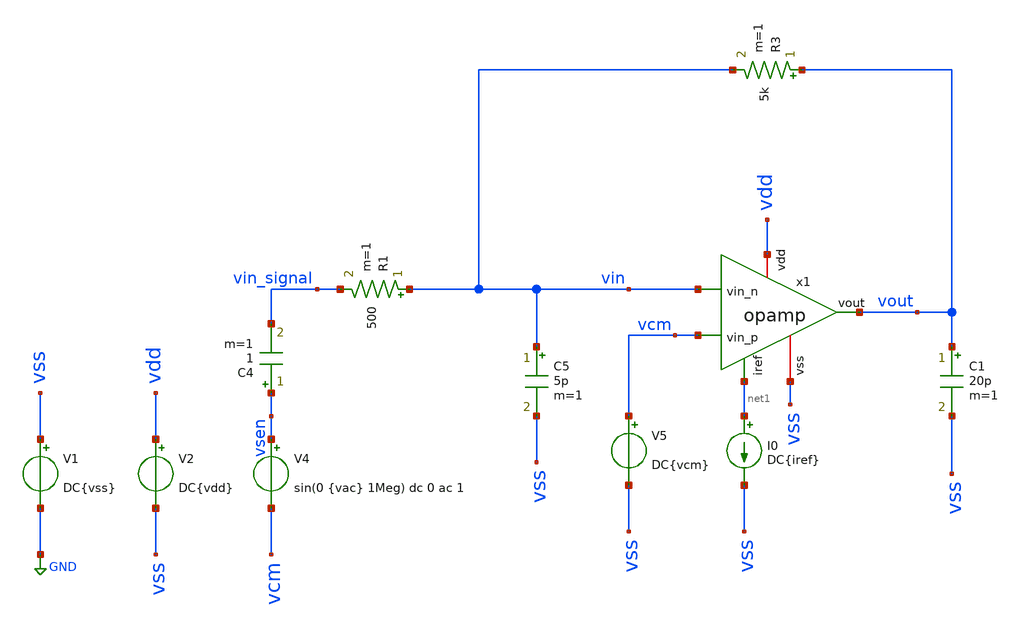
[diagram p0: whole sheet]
** sch_path: sch/opamp/opamp_closeloop.sch
**.subckt opamp_closeloop
V1 vss GND DC{vss}
V2 vdd vss DC{vdd}
V4 vsen vcm sin(0 {vac} 1Meg) dc 0 ac 1
C4 vsen vin_signal 1 m=1
I0 net1 vss DC{iref}
R1 vin vin_signal 500 m=1
R3 vout vin 5k m=1
C5 vin vss 5p m=1
C1 vout vss 20p m=1
V5 vcm vss DC{vcm}
x1 vdd net1 vin vcm vout vss opamp
**** begin user architecture code




* Circuit Parameters
.param iref = 100u
.param vdd  = 1.8
.param vss  = 0.0
.param vcm  = 0.8
.param vac  = 80m
.options TEMP = 65.0

* Include Models
.lib ~/skywater/skywater-pdk/libraries/sky130_fd_pr_ngspice/latest/models/corners/sky130.lib TT

* OP Parameters & Singals to save
.save all  @M.X1.XM1.msky130_fd_pr__pfet_01v8[id] @M.X1.XM1.msky130_fd_pr__pfet_01v8[vth] @M.X1.XM1.msky130_fd_pr__pfet_01v8[vgs] @M.X1.XM1.msky130_fd_pr__pfet_01v8[vds] @M.X1.XM1.msky130_fd_pr__pfet_01v8[vdsat] @M.X1.XM1.msky130_fd_pr__pfet_01v8[gm] @M.X1.XM1.msky130_fd_pr__pfet_01v8[gds]  @M.X1.XM2.msky130_fd_pr__pfet_01v8[id] @M.X1.XM2.msky130_fd_pr__pfet_01v8[vth] @M.X1.XM2.msky130_fd_pr__pfet_01v8[vgs] @M.X1.XM2.msky130_fd_pr__pfet_01v8[vds] @M.X1.XM2.msky130_fd_pr__pfet_01v8[vdsat] @M.X1.XM2.msky130_fd_pr__pfet_01v8[gm] @M.X1.XM2.msky130_fd_pr__pfet_01v8[gds]  @M.X1.XM3.msky130_fd_pr__nfet_01v8[id] @M.X1.XM3.msky130_fd_pr__nfet_01v8[vth] @M.X1.XM3.msky130_fd_pr__nfet_01v8[vgs] @M.X1.XM3.msky130_fd_pr__nfet_01v8[vds] @M.X1.XM3.msky130_fd_pr__nfet_01v8[vdsat] @M.X1.XM3.msky130_fd_pr__nfet_01v8[gm] @M.X1.XM3.msky130_fd_pr__nfet_01v8[gds]  @M.X1.XM4.msky130_fd_pr__nfet_01v8[id] @M.X1.XM4.msky130_fd_pr__nfet_01v8[vth] @M.X1.XM4.msky130_fd_pr__nfet_01v8[vgs] @M.X1.XM4.msky130_fd_pr__nfet_01v8[vds] @M.X1.XM4.msky130_fd_pr__nfet_01v8[vdsat] @M.X1.XM4.msky130_fd_pr__nfet_01v8[gm] @M.X1.XM4.msky130_fd_pr__nfet_01v8[gds]  @M.X1.XM5.msky130_fd_pr__pfet_01v8[id] @M.X1.XM5.msky130_fd_pr__pfet_01v8[vth] @M.X1.XM5.msky130_fd_pr__pfet_01v8[vgs] @M.X1.XM5.msky130_fd_pr__pfet_01v8[vds] @M.X1.XM5.msky130_fd_pr__pfet_01v8[vdsat] @M.X1.XM5.msky130_fd_pr__pfet_01v8[gm] @M.X1.XM5.msky130_fd_pr__pfet_01v8[gds]  @M.X1.XM6.msky130_fd_pr__nfet_01v8[id] @M.X1.XM6.msky130_fd_pr__nfet_01v8[vth] @M.X1.XM6.msky130_fd_pr__nfet_01v8[vgs] @M.X1.XM6.msky130_fd_pr__nfet_01v8[vds] @M.X1.XM6.msky130_fd_pr__nfet_01v8[vdsat] @M.X1.XM6.msky130_fd_pr__nfet_01v8[gm] @M.X1.XM6.msky130_fd_pr__nfet_01v8[gds]  @M.X1.XM7.msky130_fd_pr__pfet_01v8[id] @M.X1.XM7.msky130_fd_pr__pfet_01v8[vth] @M.X1.XM7.msky130_fd_pr__pfet_01v8[vgs] @M.X1.XM7.msky130_fd_pr__pfet_01v8[vds] @M.X1.XM7.msky130_fd_pr__pfet_01v8[vdsat] @M.X1.XM7.msky130_fd_pr__pfet_01v8[gm] @M.X1.XM7.msky130_fd_pr__pfet_01v8[gds]  @M.X1.XM8.msky130_fd_pr__pfet_01v8[id] @M.X1.XM8.msky130_fd_pr__pfet_01v8[vth] @M.X1.XM8.msky130_fd_pr__pfet_01v8[vgs] @M.X1.XM8.msky130_fd_pr__pfet_01v8[vds] @M.X1.XM8.msky130_fd_pr__pfet_01v8[vdsat] @M.X1.XM8.msky130_fd_pr__pfet_01v8[gm] @M.X1.XM8.msky130_fd_pr__pfet_01v8[gds]  @M.X1.XM9.msky130_fd_pr__nfet_01v8[id] @M.X1.XM9.msky130_fd_pr__nfet_01v8[vth] @M.X1.XM9.msky130_fd_pr__nfet_01v8[vgs] @M.X1.XM9.msky130_fd_pr__nfet_01v8[vds] @M.X1.XM9.msky130_fd_pr__nfet_01v8[vdsat] @M.X1.XM9.msky130_fd_pr__nfet_01v8[gm] @M.X1.XM9.msky130_fd_pr__nfet_01v8[gds]

*Simulations
.control
  reset
  ac dec 100 1k 10G
  setplot ac1
  meas ac GBW when vdb(vout)=0
  meas ac DCG find vdb(vout) at=1k
  plot vdb(vout) {vp(vout)*180/PI}
  *set filetype = ascii
  write opamp_closeloop_ac1.raw

  reset
  tran 0.01u 11u
  setplot tran1
  plot v(vsen) v(vout)
  *set filetype = ascii
  write opamp_closeloop_tran1.raw
  fourier 1e6 tran1.vout
  let THD_db = db(fourier11[1][3]/fourier11[1][1])
  print THD_db
  *set filetype = ascii
  write opamp_closeloop_fourier1.raw
  fft vout
  *set filetype = ascii
  write opamp_closeloop_fft1.raw
  plot mag(vout)
  plot db(mag(vout))

  reset
  noise v(vout) v4 dec 100 1k 10G 1
  save all
  *setplot noise1
  plot inoise_spectrum onoise_spectrum
  print inoise_total
  print onoise_total
  print onoise_total.m.x1.xm1.msky130_fd_pr__pfet_01v8.1overf
  print onoise_total.m.x1.xm1.msky130_fd_pr__pfet_01v8.id
  write opamp_closeloop_noise.raw

  reset
  op
  *setplot op1
  save all
  print vout
  write opamp_closeloop.raw

.endc

.end


**** end user architecture code
**.ends

* expanding   symbol:  opamp/opamp.sym # of pins=6
** sym_path: opamp/opamp.sym
** sch_path: opamp/opamp.sch
.subckt opamp vdd iref vin_n vin_p vout vss
*.iopin vdd
*.iopin vss
*.ipin vin_n
*.ipin vin_p
*.ipin iref
*.opin vout
XM1 vbn vin_n vp vp sky130_fd_pr__pfet_01v8 L=0.3 W=3 nf=1 ad='W * 0.29' as='W * 0.29' pd='2 * (W + 0.29)'
+ ps='2 * (W + 0.29)' nrd='0.29 / W' nrs='0.29 / W' sa=0 sb=0 sd=0 mult=200 m=200
XM2 voe1 vin_p vp vp sky130_fd_pr__pfet_01v8 L=0.3 W=3 nf=1 ad='W * 0.29' as='W * 0.29' pd='2 * (W + 0.29)'
+ ps='2 * (W + 0.29)' nrd='0.29 / W' nrs='0.29 / W' sa=0 sb=0 sd=0 mult=200 m=200
XM3 vbn vbn vss vss sky130_fd_pr__nfet_01v8 L=0.3 W=3 nf=1 ad='W * 0.29' as='W * 0.29' pd='2 * (W + 0.29)'
+ ps='2 * (W + 0.29)' nrd='0.29 / W' nrs='0.29 / W' sa=0 sb=0 sd=0 mult=30 m=30
XM4 voe1 vbn vss vss sky130_fd_pr__nfet_01v8 L=0.3 W=3 nf=1 ad='W * 0.29' as='W * 0.29' pd='2 * (W + 0.29)'
+ ps='2 * (W + 0.29)' nrd='0.29 / W' nrs='0.29 / W' sa=0 sb=0 sd=0 mult=30 m=30
XM5 vp iref vdd vdd sky130_fd_pr__pfet_01v8 L=0.3 W=3 nf=1 ad='W * 0.29' as='W * 0.29' pd='2 * (W + 0.29)'
+ ps='2 * (W + 0.29)' nrd='0.29 / W' nrs='0.29 / W' sa=0 sb=0 sd=0 mult=30 m=30
XM7 vout iref vdd vdd sky130_fd_pr__pfet_01v8 L=0.3 W=3 nf=1 ad='W * 0.29' as='W * 0.29' pd='2 * (W + 0.29)'
+ ps='2 * (W + 0.29)' nrd='0.29 / W' nrs='0.29 / W' sa=0 sb=0 sd=0 mult=150 m=150
XM8 iref iref vdd vdd sky130_fd_pr__pfet_01v8 L=0.3 W=3 nf=1 ad='W * 0.29' as='W * 0.29' pd='2 * (W + 0.29)'
+ ps='2 * (W + 0.29)' nrd='0.29 / W' nrs='0.29 / W' sa=0 sb=0 sd=0 mult=15 m=15
XM9 net1 vdd voe1 vss sky130_fd_pr__nfet_01v8 L=0.15 W=0.75 nf=1 ad='W * 0.29' as='W * 0.29' pd='2 * (W + 0.29)'
+ ps='2 * (W + 0.29)' nrd='0.29 / W' nrs='0.29 / W' sa=0 sb=0 sd=0 mult=6 m=6
XC1 net1 vout sky130_fd_pr__cap_mim_m3_1 W=17.55 L=15 MF=6 m=6
XM6 vout voe1 vss vss sky130_fd_pr__nfet_01v8 L=0.45 W=4.5 nf=1 ad='W * 0.29' as='W * 0.29' pd='2 * (W + 0.29)'
+ ps='2 * (W + 0.29)' nrd='0.29 / W' nrs='0.29 / W' sa=0 sb=0 sd=0 mult=150 m=150
.ends

.GLOBAL GND
.end
